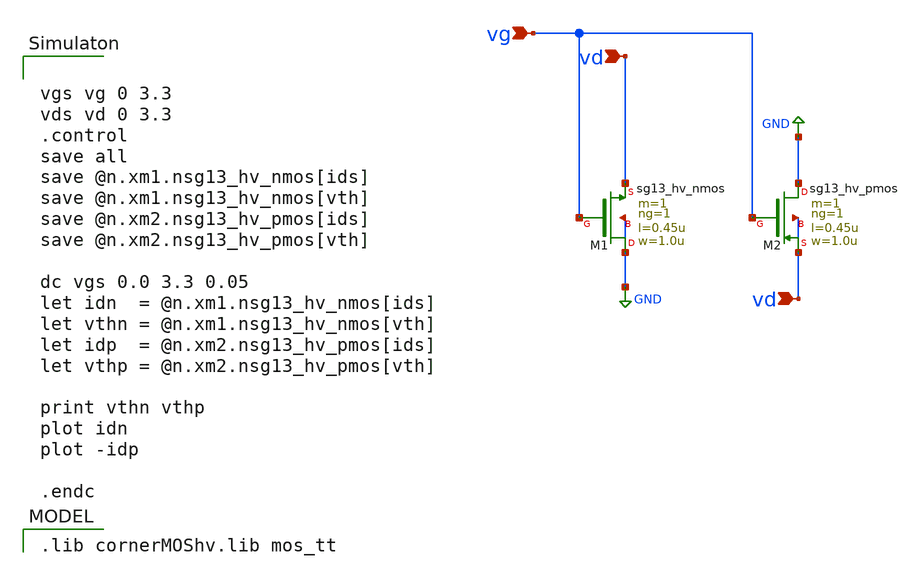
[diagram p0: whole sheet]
** sch_path: Tarea_1/xschem/DC_hv_mos.sch
**.subckt DC_hv_mos vg vd vd
*.ipin vg
*.ipin vd
*.ipin vd
XM1 GND vg vd GND sg13_hv_nmos w=1.0u l=0.45u ng=1 m=1 mm_ok=1
XM2 GND vg vd vd sg13_hv_pmos w=1.0u l=0.45u ng=1 m=1 mm_ok=1
**** begin user architecture code


vgs vg 0 3.3
vds vd 0 3.3
.control
save all
save @n.xm1.nsg13_hv_nmos[ids]
save @n.xm1.nsg13_hv_nmos[vth]
save @n.xm2.nsg13_hv_pmos[ids]
save @n.xm2.nsg13_hv_pmos[vth]

dc vgs 0.0 3.3 0.05
let idn  = @n.xm1.nsg13_hv_nmos[ids]
let vthn = @n.xm1.nsg13_hv_nmos[vth]
let idp  = @n.xm2.nsg13_hv_pmos[ids]
let vthp = @n.xm2.nsg13_hv_pmos[vth]

print vthn vthp
plot idn
plot -idp

.endc


 .lib cornerMOShv.lib mos_tt

**** end user architecture code
**.ends
.GLOBAL GND
.end
